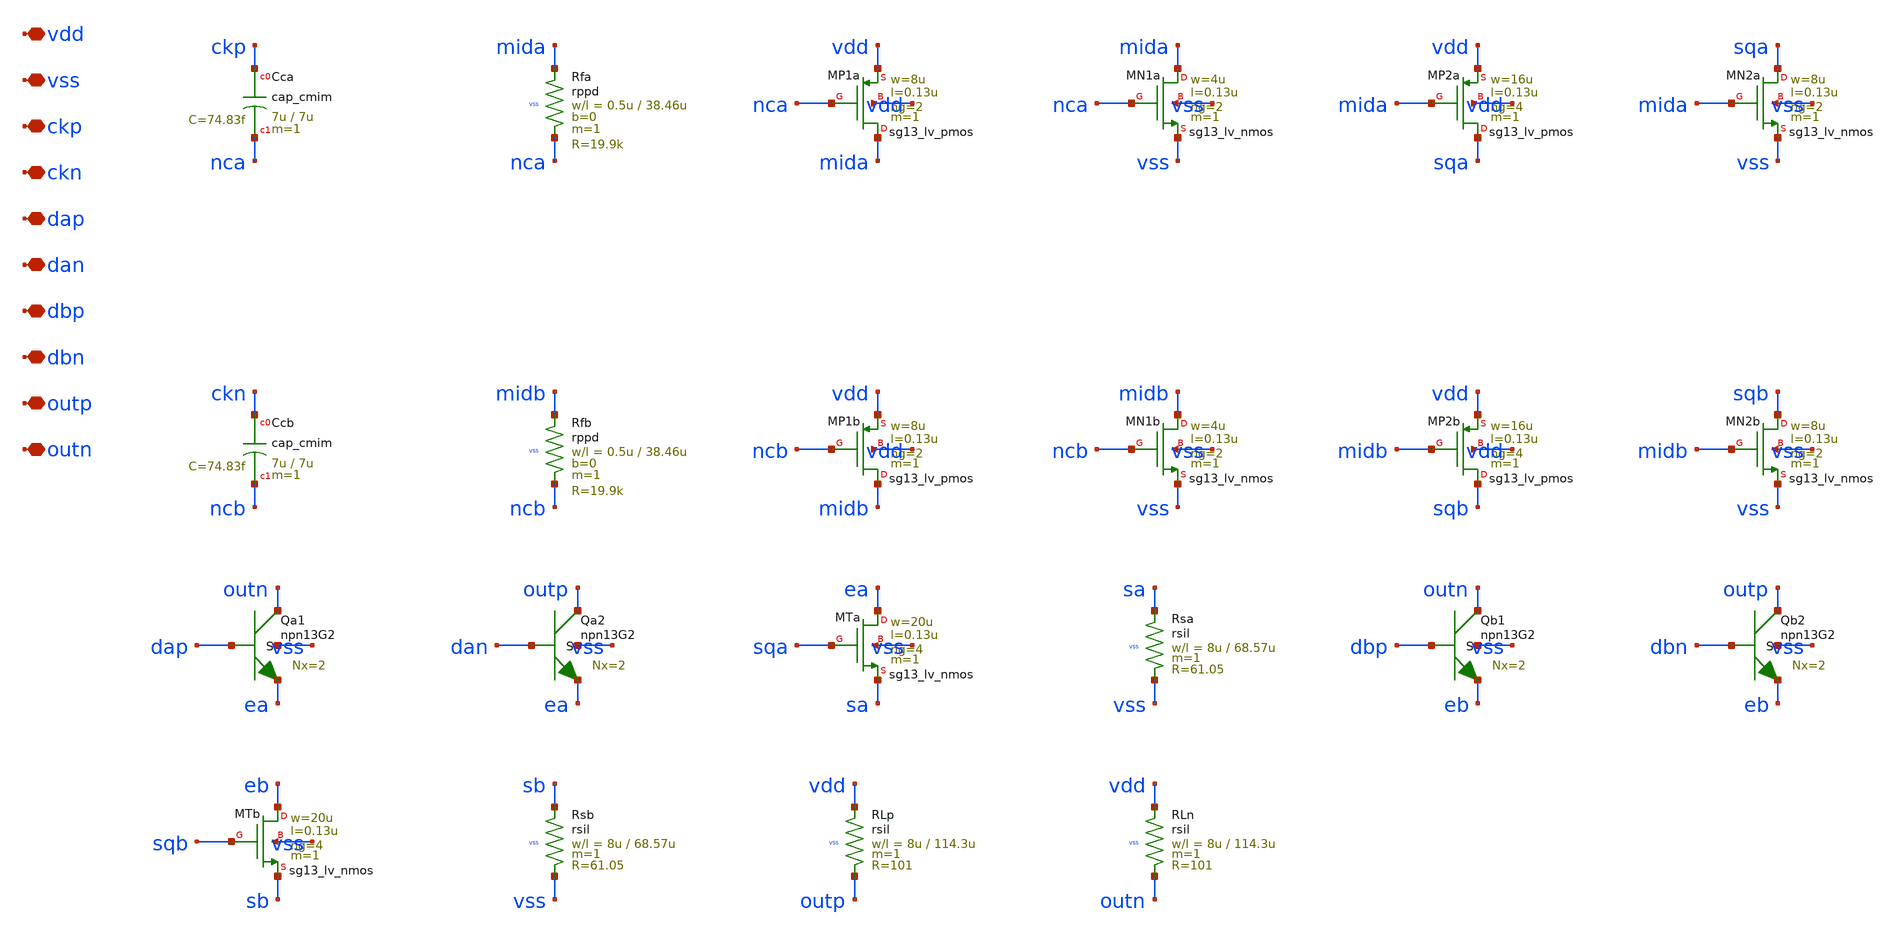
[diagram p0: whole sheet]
** sch_path: design/tx/mux2to1_cml.sch
**.subckt mux2to1_cml vdd vss ckp ckn dap dan dbp dbn outp outn
*.iopin vdd
*.iopin vss
*.iopin ckp
*.iopin ckn
*.iopin dap
*.iopin dan
*.iopin dbp
*.iopin dbn
*.iopin outp
*.iopin outn
XCca ckp nca cap_cmim w=7u l=7u m=1 mm_ok=1
XRfa mida nca vss rppd w=0.5u l=38.46u m=1 b=0 mm_ok=1
XMP1a mida nca vdd vdd sg13_lv_pmos w=8u l=0.13u ng=2 m=1 mm_ok=1
XMN1a mida nca vss vss sg13_lv_nmos w=4u l=0.13u ng=2 m=1 mm_ok=1
XMP2a sqa mida vdd vdd sg13_lv_pmos w=16u l=0.13u ng=4 m=1 mm_ok=1
XMN2a sqa mida vss vss sg13_lv_nmos w=8u l=0.13u ng=2 m=1 mm_ok=1
XCcb ckn ncb cap_cmim w=7u l=7u m=1 mm_ok=1
XRfb midb ncb vss rppd w=0.5u l=38.46u m=1 b=0 mm_ok=1
XMP1b midb ncb vdd vdd sg13_lv_pmos w=8u l=0.13u ng=2 m=1 mm_ok=1
XMN1b midb ncb vss vss sg13_lv_nmos w=4u l=0.13u ng=2 m=1 mm_ok=1
XMP2b sqb midb vdd vdd sg13_lv_pmos w=16u l=0.13u ng=4 m=1 mm_ok=1
XMN2b sqb midb vss vss sg13_lv_nmos w=8u l=0.13u ng=2 m=1 mm_ok=1
XQa1 outn dap ea vss npn13G2 Nx=2 mm_ok=1
XQa2 outp dan ea vss npn13G2 Nx=2 mm_ok=1
XMTa ea sqa sa vss sg13_lv_nmos w=20u l=0.13u ng=4 m=1 mm_ok=1
XRsa sa vss vss rsil w=8u l=68.57u m=1 mm_ok=1
XQb1 outn dbp eb vss npn13G2 Nx=2 mm_ok=1
XQb2 outp dbn eb vss npn13G2 Nx=2 mm_ok=1
XMTb eb sqb sb vss sg13_lv_nmos w=20u l=0.13u ng=4 m=1 mm_ok=1
XRsb sb vss vss rsil w=8u l=68.57u m=1 mm_ok=1
XRLp vdd outp vss rsil w=8u l=114.3u m=1 mm_ok=1
XRLn vdd outn vss rsil w=8u l=114.3u m=1 mm_ok=1
**.ends
.end
